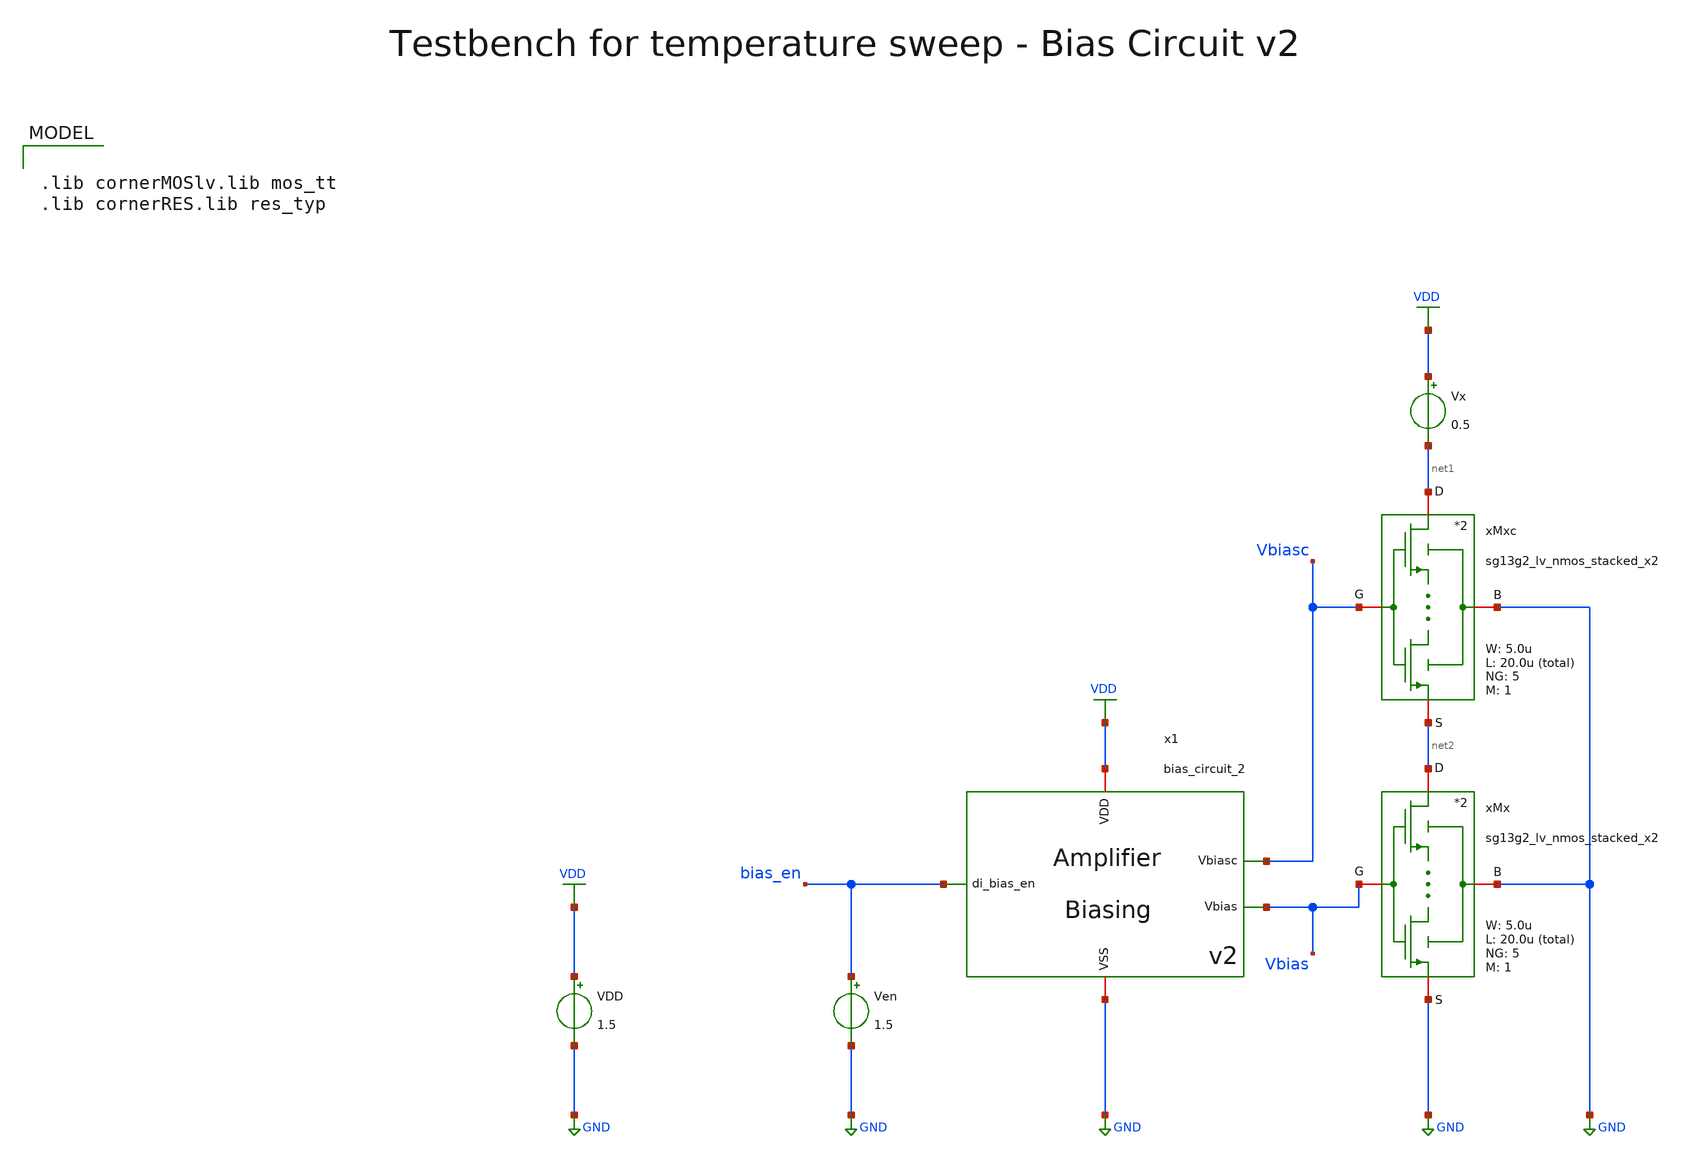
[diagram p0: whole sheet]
** sch_path: SG13G2_ATBS-ADC-main/xschem/bio_amplifier/amplifier_core/bias_circuit/bias_circuit_2/testbenches/bias_circuit_2_tb_temp.sch
**.subckt bias_circuit_2_tb_temp
Ven bias_en GND 1.5
VDD VDD GND 1.5
x1 bias_en Vbiasc VDD GND Vbias bias_circuit_2
Vx VDD net1 0.5
xMx net2 Vbias GND GND sg13g2_lv_nmos_stacked_x2 W_N=5.0u L_N=20.0u NG_N=5 M_N=1
xMxc net1 Vbiasc GND net2 sg13g2_lv_nmos_stacked_x2 W_N=5.0u L_N=20.0u NG_N=5 M_N=1
**** begin user architecture code

.lib cornerMOSlv.lib mos_tt
.lib cornerRES.lib res_typ



.param temp=27
.options savecurrents reltol=1e-3 abstol=1e-15 gmin=1e-15
.control
save all

* User Constants
* Commercial Temperature Range
let Troom = 27
let Tmin = 0
let Tmax = 70
let Tstep = 1

* Operating Point Analysis
op
remzerovec
write bias_circuit_2_tb_temp.raw
set appendwrite

* Temperature Sweep
dc temp $&Tmin $&Tmax $&Tstep
remzerovec
write bias_circuit_2_tb_temp.raw

* Plotting
plot v(Vbias) v(Vbiasc)
plot i(Vx)

* Measurements of Vbias
meas dc Vbias_Troom FIND Vbias at=Troom
meas dc Vbias_Tmin FIND Vbias at=Tmin
meas dc Vbias_Tmax FIND Vbias at=Tmax

* Calculate ppm/°C
let dVbias = Vbias_Tmax - Vbias_Tmin
print dVbias

let dT = Tmax - Tmin
print dT

let ppm_deg = (dVbias / Vbias_Troom) * (1e6 / dT)
print ppm_deg

* Measurements of Ix
meas dc Ix_Troom FIND i(Vx) at=Troom
meas dc Ix_Tmin FIND i(Vx) at=Tmin
meas dc Ix_Tmax FIND i(Vx) at=Tmax

* Calculate ppm/°C
let dIx = Ix_Tmax - Ix_Tmin
print dIx

let ppm_deg = (dIx / Ix_Troom) * (1e6 / dT)
print ppm_deg

* Write Data
set wr_vecnames
set wr_singlescale
let Ix=i(Vx)
wrdata /foss/designs/SG13G2_ATBS-ADC-main/python/plot_simulations/data/bias_circuit_2_tb_temp.txt
+ v(Vbias) v(Ix)

*quit
.endc

**** end user architecture code
**.ends

* expanding   symbol:  bio_amplifier/amplifier_core/bias_circuit/bias_circuit_2/bias_circuit_2.sym #
*+ of pins=5
** sym_path: SG13G2_ATBS-ADC-main/xschem/bio_amplifier/amplifier_core/bias_circuit/bias_circuit_2/bias_circuit_2.sym
** sch_path: SG13G2_ATBS-ADC-main/xschem/bio_amplifier/amplifier_core/bias_circuit/bias_circuit_2/bias_circuit_2.sch
.subckt bias_circuit_2 di_bias_en Vbiasc VDD VSS Vbias
*.iopin VDD
*.iopin VSS
*.opin Vbias
*.ipin di_bias_en
*.opin Vbiasc
R1 net3 VSS 3.72Meg m=1
XMDEC1 net1 Vbias net1 net1 sg13_lv_nmos w=100.0u l=40.0u ng=100 m=1 mm_ok=1
VIref net4 net8 0
.save i(viref)
VIout net9 Vbiasc 0
.save i(viout)
x1 VDD di_bias_en bias_en_n VSS inverter_lv W_P=1.0u L_P=0.13u W_N=1.0u L_N=0.13u
xMSU2 Vsu net6 VSS VSS sg13g2_lv_nmos_stacked_x4 W_N=1.0u L_N=40.0u NG_N=1 M_N=1
xMSU1 net5 Vsu VSS net6 sg13g2_lv_nmos_stacked_x4 W_N=1.0u L_N=40.0u NG_N=1 M_N=1
Vmeas1 net4 net5 0
.save i(vmeas1)
Vmeas2 Vbias net6 0
.save i(vmeas2)
XMPD1 Vgs_m34 di_bias_en net2 net2 sg13_lv_pmos w=1.0u l=0.13u ng=1 m=1 mm_ok=1
XMPD2 net4 bias_en_n Vgs_m34 net2 sg13_lv_pmos w=1.0u l=0.13u ng=1 m=1 mm_ok=1
XMPD3 Vbias bias_en_n VSS VSS sg13_lv_nmos w=1.0u l=0.13u ng=1 m=1 mm_ok=1
VIref5 net1 VSS 0
.save i(viref5)
VIdd VDD net2 0
.save i(vidd)
CSU1 net10 Vsu 35f m=1
xM1 net7 Vbias VSS net3 sg13g2_lv_nmos_stacked_x2 W_N=20.0u L_N=20.0u NG_N=20 M_N=1
xM1c net8 Vbiasc VSS net7 sg13g2_lv_nmos_stacked_x2 W_N=5.0u L_N=20.0u NG_N=5 M_N=1
xM2 Vbias Vbias VSS VSS sg13g2_lv_nmos_stacked_x2 W_N=5.0u L_N=20.0u NG_N=5 M_N=1
xM2c Vbiasc Vbiasc VSS Vbias sg13g2_lv_nmos_stacked_x2 W_N=5.0u L_N=20.0u NG_N=5 M_N=1
XMDEC2 net2 Vgs_m34 net2 net2 sg13_lv_pmos w=25.0u l=40.0u ng=25 m=1 mm_ok=1
xM3 net4 Vgs_m34 net2 net2 sg13g2_lv_pmos_stacked_x4 W_P=20.0u L_P=40.0u NG_P=20 M_P=1
xM4 net9 Vgs_m34 net2 net2 sg13g2_lv_pmos_stacked_x4 W_P=20.0u L_P=40.0u NG_P=20 M_P=1
XMPD6 Vsu di_bias_en net10 net10 sg13_lv_pmos w=1.0u l=0.13u ng=1 m=1 mm_ok=1
XMPD4 Vbiasc bias_en_n VSS VSS sg13_lv_nmos w=1.0u l=0.13u ng=1 m=1 mm_ok=1
XMPD7 Vsu bias_en_n VSS VSS sg13_lv_nmos w=1.0u l=0.13u ng=1 m=1 mm_ok=1
XMPD5 net10 bias_en_n net2 net2 sg13_lv_pmos w=1.0u l=0.13u ng=1 m=1 mm_ok=1
.ends


* expanding   symbol:  stacked_transistors/sg13g2_lv_nmos_stacked/sg13g2_lv_nmos_stacked_x2.sym # of
*+ pins=4
** sym_path: SG13G2_ATBS-ADC-main/xschem/stacked_transistors/sg13g2_lv_nmos_stacked/sg13g2_lv_nmos_stacked_x2.sym
** sch_path: SG13G2_ATBS-ADC-main/xschem/stacked_transistors/sg13g2_lv_nmos_stacked/sg13g2_lv_nmos_stacked_x2.sch
.subckt sg13g2_lv_nmos_stacked_x2 D G B S  W_N=1.0u L_N=0.45u NG_N=1 M_N=1
*.iopin D
*.iopin S
*.iopin G
*.iopin B
XM1 net1 G S B sg13_lv_nmos w=W_N l=L_N/2 ng=NG_N m=M_N mm_ok=1
XM2 D G net1 B sg13_lv_nmos w=W_N l=L_N/2 ng=NG_N m=M_N mm_ok=1
.ends


* expanding   symbol:  inverter/inverter_lv.sym # of pins=4
** sym_path: SG13G2_ATBS-ADC-main/xschem/inverter/inverter_lv.sym
** sch_path: SG13G2_ATBS-ADC-main/xschem/inverter/inverter_lv.sch
.subckt inverter_lv VDD vin vout VSS  W_P=3.0u L_P=0.13u W_N=1.0u L_N=0.13u
*.ipin vin
*.iopin VDD
*.iopin VSS
*.opin vout
XM1 vout vin VDD VDD sg13_lv_pmos w=W_P l=L_P ng=1 m=1 mm_ok=1
XM2 vout vin VSS VSS sg13_lv_nmos w=W_N l=L_N ng=1 m=1 mm_ok=1
.ends


* expanding   symbol:  stacked_transistors/sg13g2_lv_nmos_stacked/sg13g2_lv_nmos_stacked_x4.sym # of
*+ pins=4
** sym_path: SG13G2_ATBS-ADC-main/xschem/stacked_transistors/sg13g2_lv_nmos_stacked/sg13g2_lv_nmos_stacked_x4.sym
** sch_path: SG13G2_ATBS-ADC-main/xschem/stacked_transistors/sg13g2_lv_nmos_stacked/sg13g2_lv_nmos_stacked_x4.sch
.subckt sg13g2_lv_nmos_stacked_x4 D G B S  W_N=1.0u L_N=0.45u NG_N=1 M_N=1
*.iopin D
*.iopin S
*.iopin G
*.iopin B
XM1 net1 G S B sg13_lv_nmos w=W_N l=L_N/4 ng=NG_N m=M_N mm_ok=1
XM2 net3 G net1 B sg13_lv_nmos w=W_N l=L_N/4 ng=NG_N m=M_N mm_ok=1
XM3 net2 G net3 B sg13_lv_nmos w=W_N l=L_N/4 ng=NG_N m=M_N mm_ok=1
XM4 D G net2 B sg13_lv_nmos w=W_N l=L_N/4 ng=NG_N m=M_N mm_ok=1
.ends


* expanding   symbol:  stacked_transistors/sg13g2_lv_pmos_stacked/sg13g2_lv_pmos_stacked_x4.sym # of
*+ pins=4
** sym_path: SG13G2_ATBS-ADC-main/xschem/stacked_transistors/sg13g2_lv_pmos_stacked/sg13g2_lv_pmos_stacked_x4.sym
** sch_path: SG13G2_ATBS-ADC-main/xschem/stacked_transistors/sg13g2_lv_pmos_stacked/sg13g2_lv_pmos_stacked_x4.sch
.subckt sg13g2_lv_pmos_stacked_x4 D G B S  W_P=1.0u L_P=0.45u NG_P=1 M_P=1
*.iopin D
*.iopin S
*.iopin G
*.iopin B
XM1 net1 G S B sg13_lv_pmos w=W_P l=L_P/4 ng=NG_P m=M_P mm_ok=1
XM2 net3 G net1 B sg13_lv_pmos w=W_P l=L_P/4 ng=NG_P m=M_P mm_ok=1
XM3 net2 G net3 B sg13_lv_pmos w=W_P l=L_P/4 ng=NG_P m=M_P mm_ok=1
XM4 D G net2 B sg13_lv_pmos w=W_P l=L_P/4 ng=NG_P m=M_P mm_ok=1
.ends

.GLOBAL GND
.GLOBAL VDD
.end
